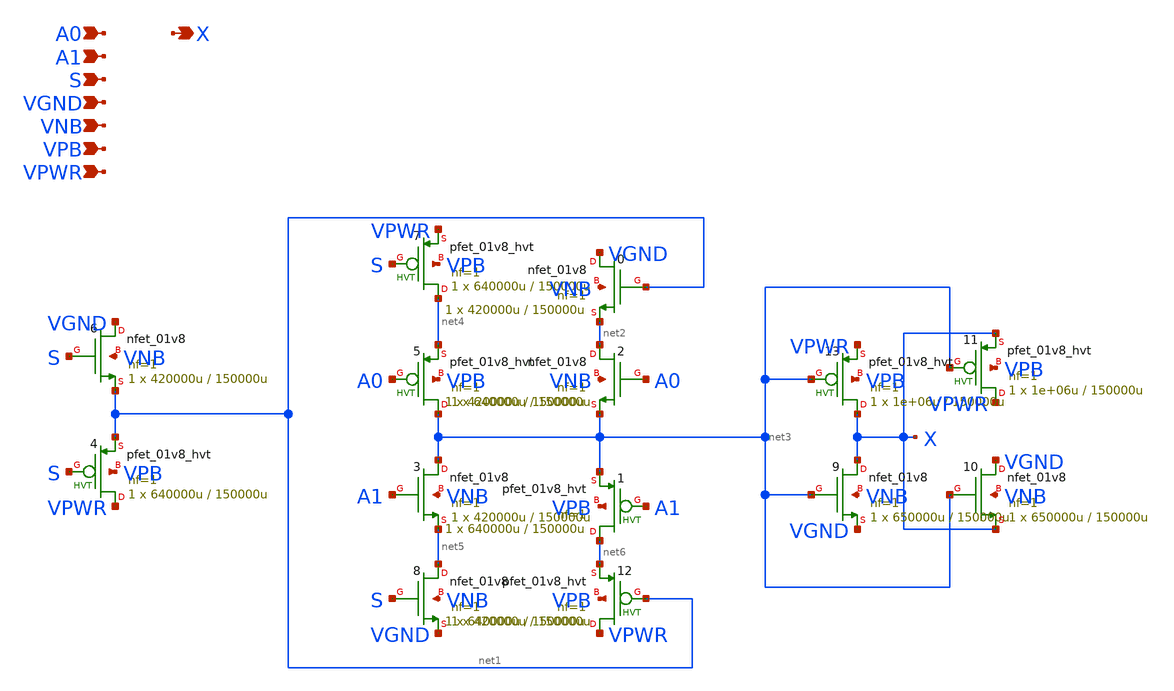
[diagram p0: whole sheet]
** sch_path: schematics/mux2/sky130_fd_sc_hd__mux2_2.sch
**.subckt sky130_fd_sc_hd__mux2_2 A0 A1 S VGND VNB VPB VPWR X
*.ipin A0
*.ipin A1
*.ipin S
*.ipin VGND
*.ipin VNB
*.ipin VPB
*.ipin VPWR
*.opin X
X0 VGND net1 net2 VNB sky130_fd_pr__nfet_01v8 L=150000u W=420000u nf=1 ad='int((1 + 1)/2) * 420000u / 1 * 0.29'
+ as='int((1 + 2)/2) * 420000u / 1 * 0.29' pd='2*int((1 + 1)/2) * (420000u / 1 + 0.29)' ps='2*int((1 + 2)/2) * (420000u / 1 + 0.29)'
+ nrd='0.29 / 420000u ' nrs='0.29 / 420000u ' sa=0 sb=0 sd=0 mult=1 m=1
X6 VGND S net1 VNB sky130_fd_pr__nfet_01v8 L=150000u W=420000u nf=1 ad='int((1 + 1)/2) * 420000u / 1 * 0.29'
+ as='int((1 + 2)/2) * 420000u / 1 * 0.29' pd='2*int((1 + 1)/2) * (420000u / 1 + 0.29)' ps='2*int((1 + 2)/2) * (420000u / 1 + 0.29)'
+ nrd='0.29 / 420000u ' nrs='0.29 / 420000u ' sa=0 sb=0 sd=0 mult=1 m=1
X4 VPWR S net1 VPB sky130_fd_pr__pfet_01v8_hvt L=150000u W=640000u nf=1 ad='int((1 + 1)/2) * 640000u / 1 * 0.29'
+ as='int((1 + 2)/2) * 640000u / 1 * 0.29' pd='2*int((1 + 1)/2) * (640000u / 1 + 0.29)' ps='2*int((1 + 2)/2) * (640000u / 1 + 0.29)'
+ nrd='0.29 / 640000u ' nrs='0.29 / 640000u ' sa=0 sb=0 sd=0 mult=1 m=1
X12 VPWR net1 net6 VPB sky130_fd_pr__pfet_01v8_hvt L=150000u W=640000u nf=1 ad='int((1 + 1)/2) * 640000u / 1 * 0.29'
+ as='int((1 + 2)/2) * 640000u / 1 * 0.29' pd='2*int((1 + 1)/2) * (640000u / 1 + 0.29)' ps='2*int((1 + 2)/2) * (640000u / 1 + 0.29)'
+ nrd='0.29 / 640000u ' nrs='0.29 / 640000u ' sa=0 sb=0 sd=0 mult=1 m=1
X1 net6 A1 net3 VPB sky130_fd_pr__pfet_01v8_hvt L=150000u W=640000u nf=1 ad='int((1 + 1)/2) * 640000u / 1 * 0.29'
+ as='int((1 + 2)/2) * 640000u / 1 * 0.29' pd='2*int((1 + 1)/2) * (640000u / 1 + 0.29)' ps='2*int((1 + 2)/2) * (640000u / 1 + 0.29)'
+ nrd='0.29 / 640000u ' nrs='0.29 / 640000u ' sa=0 sb=0 sd=0 mult=1 m=1
X2 net2 A0 net3 VNB sky130_fd_pr__nfet_01v8 L=150000u W=420000u nf=1 ad='int((1 + 1)/2) * 420000u / 1 * 0.29'
+ as='int((1 + 2)/2) * 420000u / 1 * 0.29' pd='2*int((1 + 1)/2) * (420000u / 1 + 0.29)' ps='2*int((1 + 2)/2) * (420000u / 1 + 0.29)'
+ nrd='0.29 / 420000u ' nrs='0.29 / 420000u ' sa=0 sb=0 sd=0 mult=1 m=1
X3 net3 A1 net5 VNB sky130_fd_pr__nfet_01v8 L=150000u W=420000u nf=1 ad='int((1 + 1)/2) * 420000u / 1 * 0.29'
+ as='int((1 + 2)/2) * 420000u / 1 * 0.29' pd='2*int((1 + 1)/2) * (420000u / 1 + 0.29)' ps='2*int((1 + 2)/2) * (420000u / 1 + 0.29)'
+ nrd='0.29 / 420000u ' nrs='0.29 / 420000u ' sa=0 sb=0 sd=0 mult=1 m=1
X5 net3 A0 net4 VPB sky130_fd_pr__pfet_01v8_hvt L=150000u W=640000u nf=1 ad='int((1 + 1)/2) * 640000u / 1 * 0.29'
+ as='int((1 + 2)/2) * 640000u / 1 * 0.29' pd='2*int((1 + 1)/2) * (640000u / 1 + 0.29)' ps='2*int((1 + 2)/2) * (640000u / 1 + 0.29)'
+ nrd='0.29 / 640000u ' nrs='0.29 / 640000u ' sa=0 sb=0 sd=0 mult=1 m=1
X7 net4 S VPWR VPB sky130_fd_pr__pfet_01v8_hvt L=150000u W=640000u nf=1 ad='int((1 + 1)/2) * 640000u / 1 * 0.29'
+ as='int((1 + 2)/2) * 640000u / 1 * 0.29' pd='2*int((1 + 1)/2) * (640000u / 1 + 0.29)' ps='2*int((1 + 2)/2) * (640000u / 1 + 0.29)'
+ nrd='0.29 / 640000u ' nrs='0.29 / 640000u ' sa=0 sb=0 sd=0 mult=1 m=1
X8 net5 S VGND VNB sky130_fd_pr__nfet_01v8 L=150000u W=420000u nf=1 ad='int((1 + 1)/2) * 420000u / 1 * 0.29'
+ as='int((1 + 2)/2) * 420000u / 1 * 0.29' pd='2*int((1 + 1)/2) * (420000u / 1 + 0.29)' ps='2*int((1 + 2)/2) * (420000u / 1 + 0.29)'
+ nrd='0.29 / 420000u ' nrs='0.29 / 420000u ' sa=0 sb=0 sd=0 mult=1 m=1
X13 X net3 VPWR VPB sky130_fd_pr__pfet_01v8_hvt L=150000u W=1e+06u nf=1 ad='int((1 + 1)/2) * 1e+06u / 1 * 0.29'
+ as='int((1 + 2)/2) * 1e+06u / 1 * 0.29' pd='2*int((1 + 1)/2) * (1e+06u / 1 + 0.29)' ps='2*int((1 + 2)/2) * (1e+06u / 1 + 0.29)'
+ nrd='0.29 / 1e+06u ' nrs='0.29 / 1e+06u ' sa=0 sb=0 sd=0 mult=1 m=1
X9 X net3 VGND VNB sky130_fd_pr__nfet_01v8 L=150000u W=650000u nf=1 ad='int((1 + 1)/2) * 650000u / 1 * 0.29'
+ as='int((1 + 2)/2) * 650000u / 1 * 0.29' pd='2*int((1 + 1)/2) * (650000u / 1 + 0.29)' ps='2*int((1 + 2)/2) * (650000u / 1 + 0.29)'
+ nrd='0.29 / 650000u ' nrs='0.29 / 650000u ' sa=0 sb=0 sd=0 mult=1 m=1
X11 VPWR net3 X VPB sky130_fd_pr__pfet_01v8_hvt L=150000u W=1e+06u nf=1 ad='int((1 + 1)/2) * 1e+06u / 1 * 0.29'
+ as='int((1 + 2)/2) * 1e+06u / 1 * 0.29' pd='2*int((1 + 1)/2) * (1e+06u / 1 + 0.29)' ps='2*int((1 + 2)/2) * (1e+06u / 1 + 0.29)'
+ nrd='0.29 / 1e+06u ' nrs='0.29 / 1e+06u ' sa=0 sb=0 sd=0 mult=1 m=1
X10 VGND net3 X VNB sky130_fd_pr__nfet_01v8 L=150000u W=650000u nf=1 ad='int((1 + 1)/2) * 650000u / 1 * 0.29'
+ as='int((1 + 2)/2) * 650000u / 1 * 0.29' pd='2*int((1 + 1)/2) * (650000u / 1 + 0.29)' ps='2*int((1 + 2)/2) * (650000u / 1 + 0.29)'
+ nrd='0.29 / 650000u ' nrs='0.29 / 650000u ' sa=0 sb=0 sd=0 mult=1 m=1
**.ends
.end
